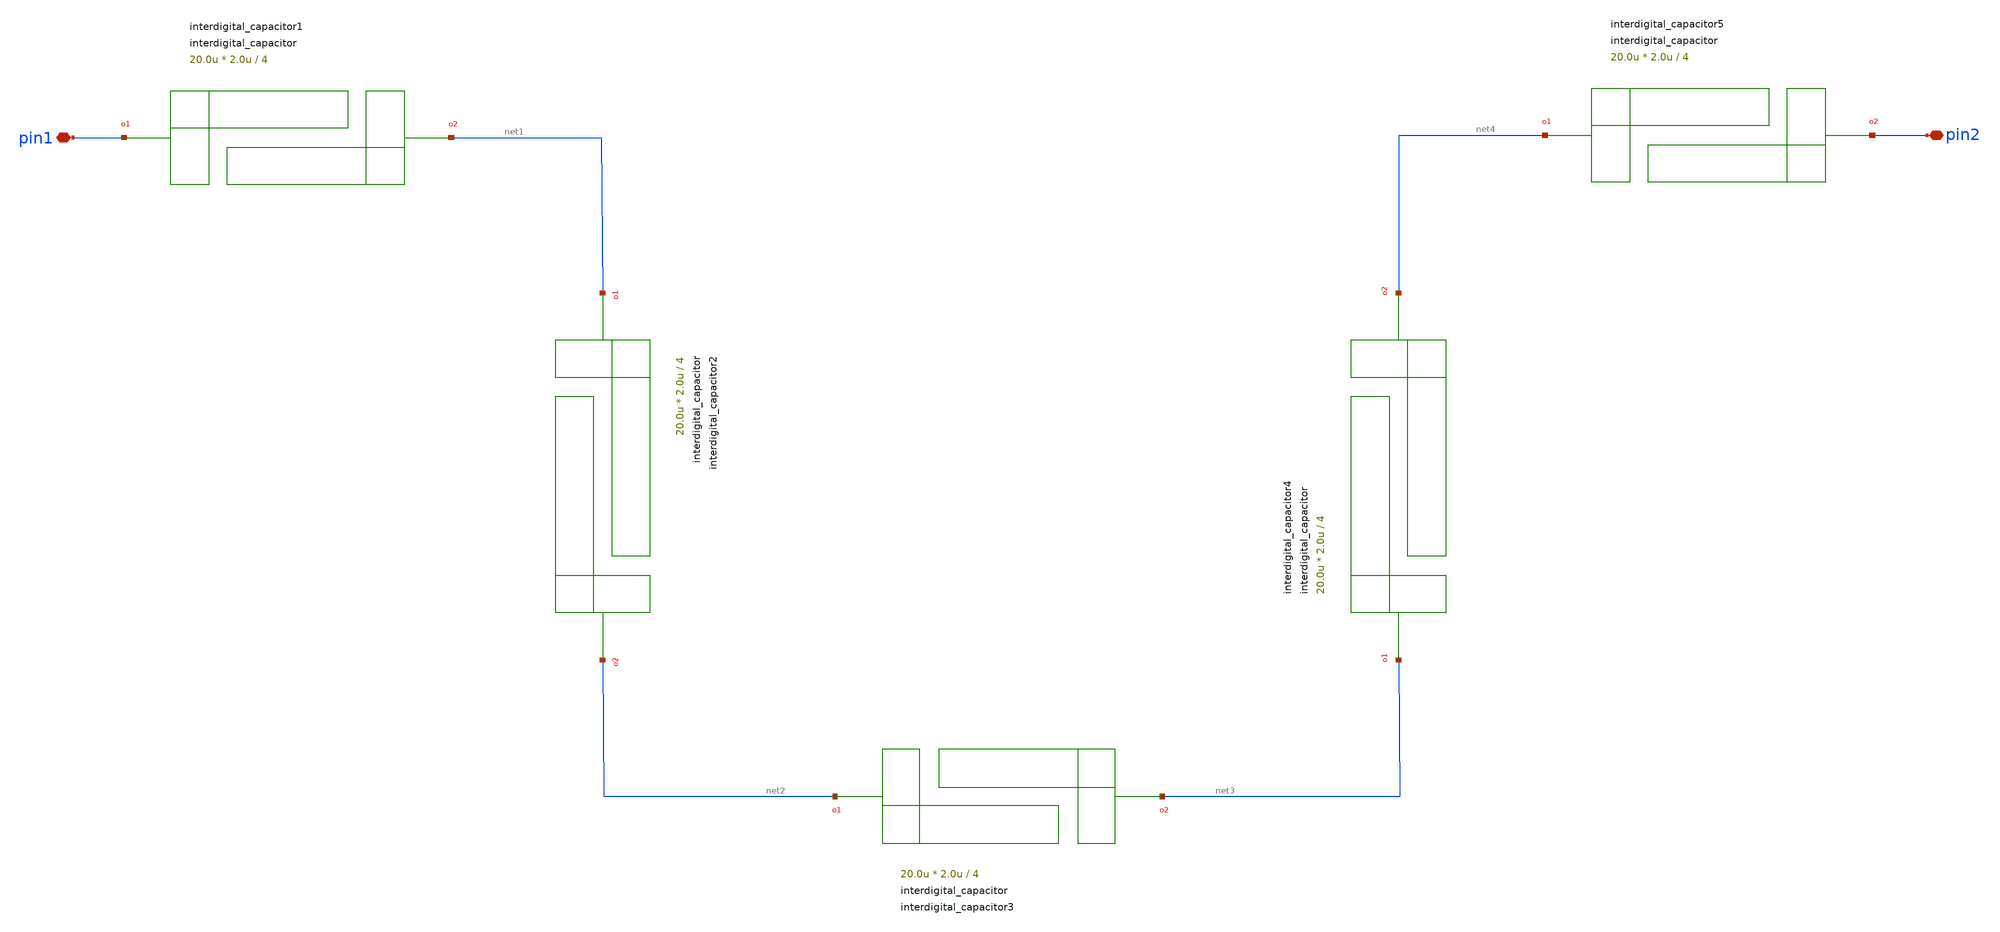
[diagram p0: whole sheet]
** sch_path: xschem/tests/test_sch/test_interdigital_capacitor.sch
* Copyright (c) 2024, Mabrains LLC
* Licensed under the GNU Lesser General Public License, Version 3.0 (the "License");
* you may not use this file except in compliance with the License.
* GNU Lesser General Public License
* Version 3, 29 June 2007
* This program is free software: you can redistribute it and/or modify
* it under the terms of the GNU Lesser General Public License as published
* by the Free Software Foundation, either version 3 of the License, or
* (at your option) any later version.
* This program is distributed in the hope that it will be useful,
* but WITHOUT ANY WARRANTY; without even the implied warranty of
* MERCHANTABILITY or FITNESS FOR A PARTICULAR PURPOSE.  See the
* GNU Lesser General Public License for more details.
* You should have received a copy of the GNU Lesser General Public License
* along with this program.  If not, see <https://www.gnu.org/licenses/>.
* SPDX-License-Identifier: LGPL-3.0
**.subckt test_interdigital_capacitor pin1 pin2
*.iopin pin1
*.iopin pin2
Pinterdigital_capacitor1 pin1 net1 interdigital_capacitor fingers=4 finger_length=20.0u
+ finger_gap=2.0u thickness=5.0u
Pinterdigital_capacitor2 net1 net2 interdigital_capacitor fingers=4 finger_length=20.0u
+ finger_gap=2.0u thickness=5.0u
Pinterdigital_capacitor3 net2 net3 interdigital_capacitor fingers=4 finger_length=20.0u
+ finger_gap=2.0u thickness=5.0u
Pinterdigital_capacitor4 net3 net4 interdigital_capacitor fingers=4 finger_length=20.0u
+ finger_gap=2.0u thickness=5.0u
Pinterdigital_capacitor5 net4 pin2 interdigital_capacitor fingers=4 finger_length=20.0u
+ finger_gap=2.0u thickness=5.0u
**.ends
.end
